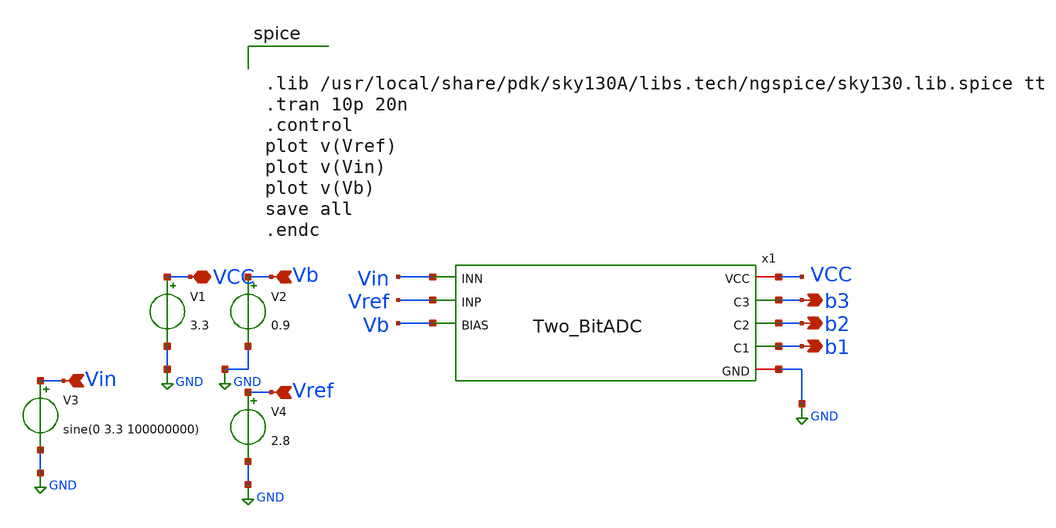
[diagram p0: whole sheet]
** sch_path: week7/pre-layout/tb_2bitADC.sch
**.subckt tb_2bitADC b3 b2 b1 Vb Vref Vin VCC
*.opin b3
*.opin b2
*.opin b1
*.ipin Vb
*.ipin Vref
*.ipin Vin
*.iopin VCC
x1 Vin Vref VCC Vb b3 b2 b1 GND Two_BitADC
V1 VCC GND 3.3
V2 Vb GND 0.9
V3 Vin GND sine(0 3.3 100000000)
V4 Vref GND 2.8
**** begin user architecture code


.lib /usr/local/share/pdk/sky130A/libs.tech/ngspice/sky130.lib.spice tt
.tran 10p 20n
.control
plot v(Vref)
plot v(Vin)
plot v(Vb)
save all
.endc

**** end user architecture code
**.ends

* expanding   symbol:  Two_BitADC.sym # of pins=8
** sym_path: week7/pre-layout/Two_BitADC.sym
** sch_path: week7/pre-layout/Two_BitADC.sch
.subckt Two_BitADC INN INP VCC BIAS C3 C2 C1 GND
*.iopin VCC
*.ipin BIAS
*.opin C3
*.opin C2
*.opin C1
*.ipin INN
*.ipin INP
*.iopin GND
x1 VCC C3 net1 INN GND BIAS comp
XR1 net1 INP INP sky130_fd_pr__res_generic_pd W=10 L=5.2 mult=1 m=1
XR2 net2 net1 net1 sky130_fd_pr__res_generic_pd W=10 L=5.2 mult=1 m=1
XR3 net3 net2 net2 sky130_fd_pr__res_generic_pd W=10 L=5.2 mult=1 m=1
XR4 GND net3 net3 sky130_fd_pr__res_generic_pd W=10 L=5.2 mult=1 m=1
x2 VCC C2 net2 INN GND BIAS comp
x3 VCC C1 net3 INN GND BIAS comp
.ends


* expanding   symbol:  comp.sym # of pins=6
** sym_path: week7/pre-layout/comp.sym
** sch_path: week7/pre-layout/comp.sch
.subckt comp VCC OUT INN INP GND BIAS
*.ipin BIAS
*.iopin VCC
*.iopin GND
*.opin OUT
*.ipin INN
*.ipin INP
XM1 net3 net3 VCC VCC sky130_fd_pr__pfet_01v8 L=0.15 W=0.84 nf=1 ad='int((nf+1)/2) * W/nf * 0.29' as='int((nf+2)/2) * W/nf * 0.29'
+ pd='2*int((nf+1)/2) * (W/nf + 0.29)' ps='2*int((nf+2)/2) * (W/nf + 0.29)' nrd='0.29 / W' nrs='0.29 / W'
+ sa=0 sb=0 sd=0 mult=1 m=1
XM3 net3 INN net1 GND sky130_fd_pr__nfet_01v8 L=0.15 W=0.84 nf=1 ad='int((nf+1)/2) * W/nf * 0.29' as='int((nf+2)/2) * W/nf * 0.29'
+ pd='2*int((nf+1)/2) * (W/nf + 0.29)' ps='2*int((nf+2)/2) * (W/nf + 0.29)' nrd='0.29 / W' nrs='0.29 / W'
+ sa=0 sb=0 sd=0 mult=1 m=1
XM12 net1 BIAS GND GND sky130_fd_pr__nfet_01v8 L=0.15 W=0.84 nf=1 ad='int((nf+1)/2) * W/nf * 0.29' as='int((nf+2)/2) * W/nf * 0.29'
+ pd='2*int((nf+1)/2) * (W/nf + 0.29)' ps='2*int((nf+2)/2) * (W/nf + 0.29)' nrd='0.29 / W' nrs='0.29 / W'
+ sa=0 sb=0 sd=0 mult=1 m=1
XM2 net2 net3 VCC VCC sky130_fd_pr__pfet_01v8 L=0.15 W=0.84 nf=1 ad='int((nf+1)/2) * W/nf * 0.29' as='int((nf+2)/2) * W/nf * 0.29'
+ pd='2*int((nf+1)/2) * (W/nf + 0.29)' ps='2*int((nf+2)/2) * (W/nf + 0.29)' nrd='0.29 / W' nrs='0.29 / W'
+ sa=0 sb=0 sd=0 mult=1 m=1
XM4 net2 INP net1 GND sky130_fd_pr__nfet_01v8 L=0.15 W=0.84 nf=1 ad='int((nf+1)/2) * W/nf * 0.29' as='int((nf+2)/2) * W/nf * 0.29'
+ pd='2*int((nf+1)/2) * (W/nf + 0.29)' ps='2*int((nf+2)/2) * (W/nf + 0.29)' nrd='0.29 / W' nrs='0.29 / W'
+ sa=0 sb=0 sd=0 mult=1 m=1
XM5 net4 net2 VCC VCC sky130_fd_pr__pfet_01v8 L=0.15 W=0.84 nf=1 ad='int((nf+1)/2) * W/nf * 0.29' as='int((nf+2)/2) * W/nf * 0.29'
+ pd='2*int((nf+1)/2) * (W/nf + 0.29)' ps='2*int((nf+2)/2) * (W/nf + 0.29)' nrd='0.29 / W' nrs='0.29 / W'
+ sa=0 sb=0 sd=0 mult=1 m=1
XM6 net4 net2 GND GND sky130_fd_pr__nfet_01v8 L=0.15 W=0.84 nf=1 ad='int((nf+1)/2) * W/nf * 0.29' as='int((nf+2)/2) * W/nf * 0.29'
+ pd='2*int((nf+1)/2) * (W/nf + 0.29)' ps='2*int((nf+2)/2) * (W/nf + 0.29)' nrd='0.29 / W' nrs='0.29 / W'
+ sa=0 sb=0 sd=0 mult=1 m=1
XM7 net5 net4 GND GND sky130_fd_pr__nfet_01v8 L=0.15 W=0.84 nf=1 ad='int((nf+1)/2) * W/nf * 0.29' as='int((nf+2)/2) * W/nf * 0.29'
+ pd='2*int((nf+1)/2) * (W/nf + 0.29)' ps='2*int((nf+2)/2) * (W/nf + 0.29)' nrd='0.29 / W' nrs='0.29 / W'
+ sa=0 sb=0 sd=0 mult=1 m=1
XM8 OUT net5 GND GND sky130_fd_pr__nfet_01v8 L=0.15 W=0.84 nf=1 ad='int((nf+1)/2) * W/nf * 0.29' as='int((nf+2)/2) * W/nf * 0.29'
+ pd='2*int((nf+1)/2) * (W/nf + 0.29)' ps='2*int((nf+2)/2) * (W/nf + 0.29)' nrd='0.29 / W' nrs='0.29 / W'
+ sa=0 sb=0 sd=0 mult=1 m=1
XM9 net5 net4 VCC VCC sky130_fd_pr__pfet_01v8 L=0.15 W=0.84 nf=1 ad='int((nf+1)/2) * W/nf * 0.29' as='int((nf+2)/2) * W/nf * 0.29'
+ pd='2*int((nf+1)/2) * (W/nf + 0.29)' ps='2*int((nf+2)/2) * (W/nf + 0.29)' nrd='0.29 / W' nrs='0.29 / W'
+ sa=0 sb=0 sd=0 mult=1 m=1
XM10 OUT net5 VCC VCC sky130_fd_pr__pfet_01v8 L=0.15 W=0.84 nf=1 ad='int((nf+1)/2) * W/nf * 0.29' as='int((nf+2)/2) * W/nf * 0.29'
+ pd='2*int((nf+1)/2) * (W/nf + 0.29)' ps='2*int((nf+2)/2) * (W/nf + 0.29)' nrd='0.29 / W' nrs='0.29 / W'
+ sa=0 sb=0 sd=0 mult=1 m=1
.ends

.GLOBAL GND
.end
